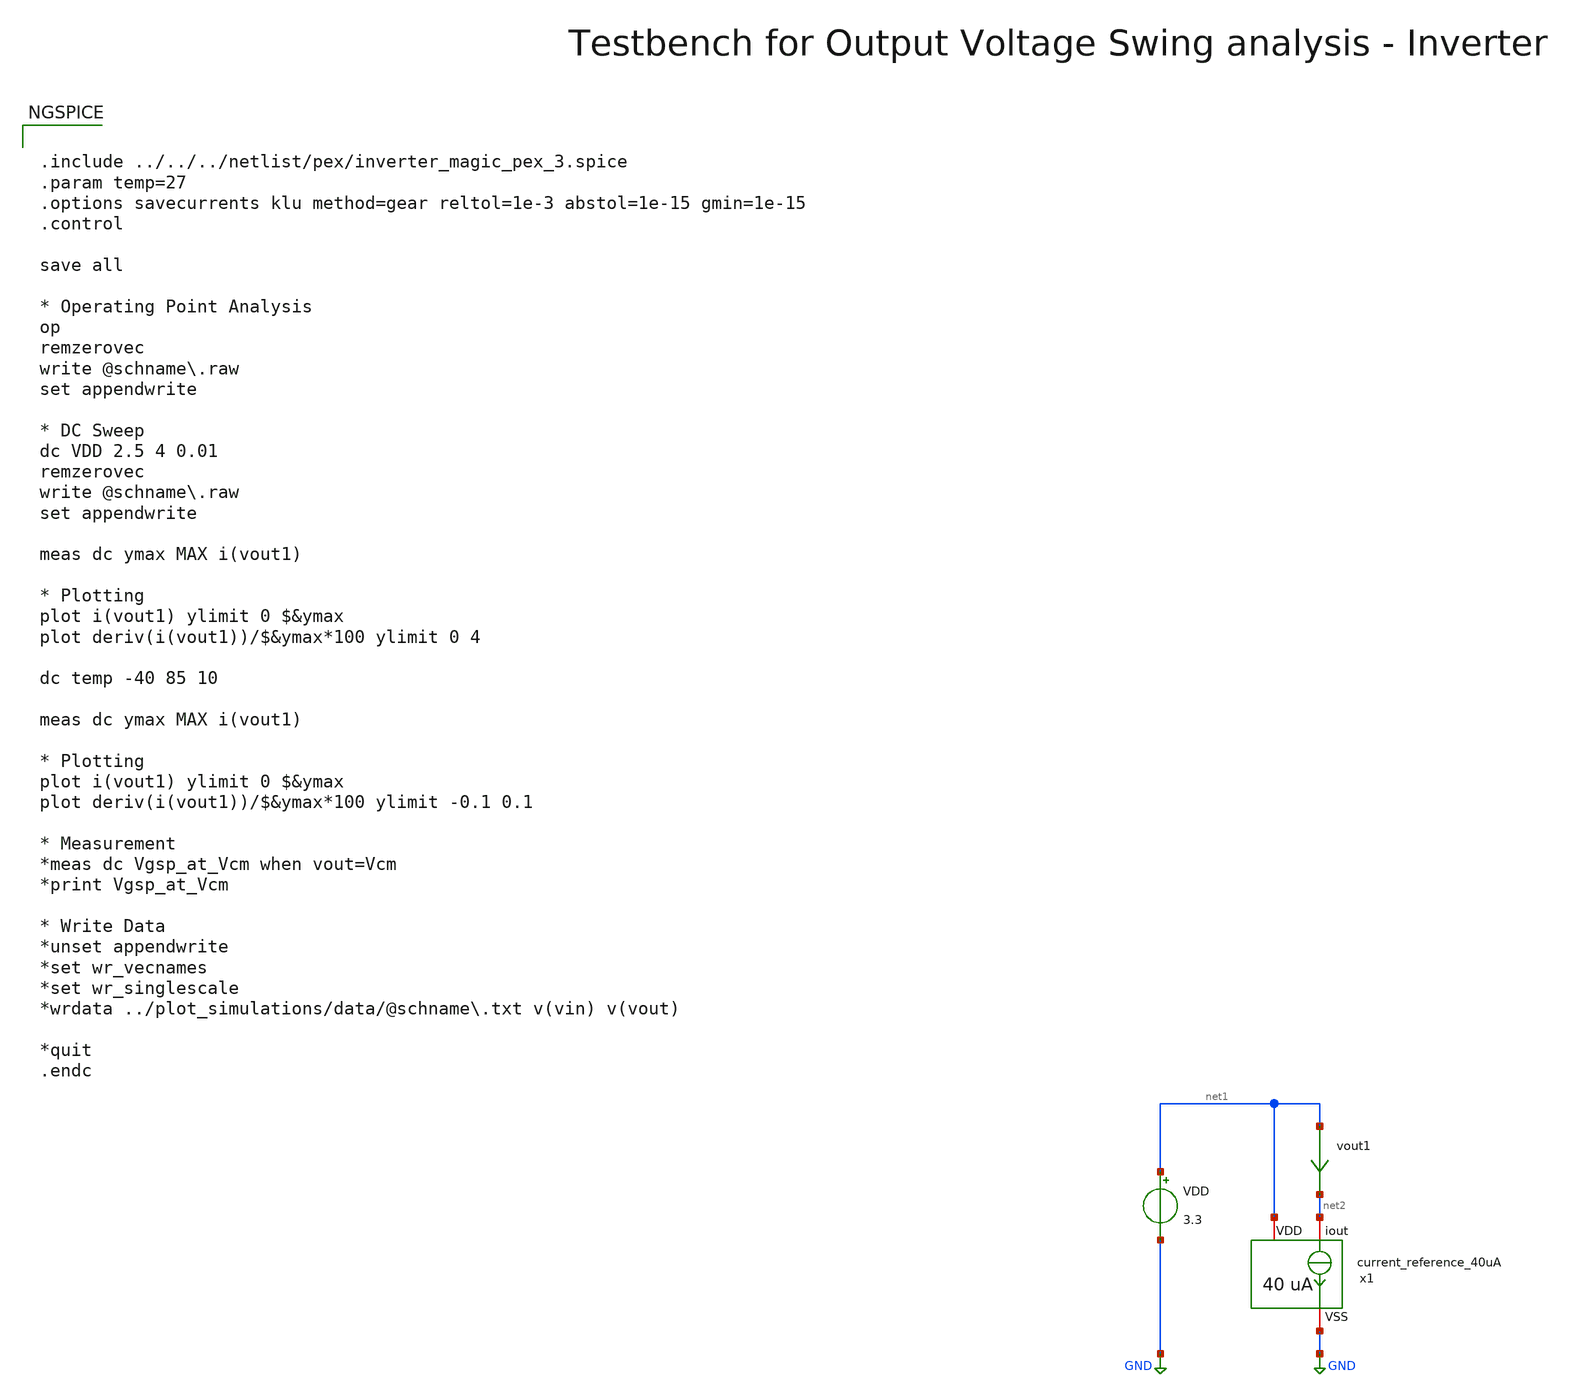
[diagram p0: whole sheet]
** sch_path: macros/heichips26_vcr/macros/switched_capacitor/testbenches/xschem/tb_current_reference_dc.sch
**.subckt tb_current_reference_dc
VDD net1 GND 3.3
vout1 net1 net2 0
.save i(vout1)
x1 net1 net2 GND current_reference_40uA
**** begin user architecture code


.include ../../../netlist/pex/inverter_magic_pex_3.spice
.param temp=27
.options savecurrents klu method=gear reltol=1e-3 abstol=1e-15 gmin=1e-15
.control

save all

* Operating Point Analysis
op
remzerovec
write @schname\.raw
set appendwrite

* DC Sweep
dc VDD 2.5 4 0.01
remzerovec
write @schname\.raw
set appendwrite

meas dc ymax MAX i(vout1)

* Plotting
plot i(vout1) ylimit 0 $&ymax
plot deriv(i(vout1))/$&ymax*100 ylimit 0 4

dc temp -40 85 10

meas dc ymax MAX i(vout1)

* Plotting
plot i(vout1) ylimit 0 $&ymax
plot deriv(i(vout1))/$&ymax*100 ylimit -0.1 0.1

* Measurement
*meas dc Vgsp_at_Vcm when vout=Vcm
*print Vgsp_at_Vcm

* Write Data
*unset appendwrite
*set wr_vecnames
*set wr_singlescale
*wrdata ../plot_simulations/data/@schname\.txt v(vin) v(vout)

*quit
.endc



.lib cornerMOSlv.lib mos_tt
.lib cornerMOShv.lib mos_tt
.lib cornerRES.lib res_typ
.lib cornerDIO.lib dio_tt

**** end user architecture code
**.ends

* expanding   symbol:  current_reference_40uA.sym # of pins=3
** sym_path: macros/heichips26_vcr/macros/switched_capacitor/schematic/xschem/current_reference_40uA.sym
** sch_path: macros/heichips26_vcr/macros/switched_capacitor/schematic/xschem/current_reference_40uA.sch
.subckt current_reference_40uA VDD iout VSS
*.iopin VSS
*.iopin VDD
*.iopin iout
XM8 net2 net2 VSS VSS sg13_hv_nmos w=n_w l=n_l ng=1 m=1 mm_ok=1
XM6 net2 net1 VDD VDD sg13_hv_pmos w=p_w l=p_l ng=1 m=1 mm_ok=1
XM1 net1 net1 VDD VDD sg13_hv_pmos w=p_w l=p_l ng=1 m=1 mm_ok=1
XM3 net1 net2 net3 VSS sg13_hv_nmos w=n_w l=n_l ng=1 m=1 mm_ok=1
XR2 net4 VSS VSS rppd w=2e-6 l=21.9e-6 m=1 b=0 mm_ok=1
XM2 net1 net2 net3 VSS sg13_hv_nmos w=n_w l=n_l ng=1 m=1 mm_ok=1
XM4 net1 net2 net3 VSS sg13_hv_nmos w=n_w l=n_l ng=1 m=1 mm_ok=1
XM5 net1 net2 net3 VSS sg13_hv_nmos w=n_w l=n_l ng=1 m=1 mm_ok=1
XM7 iout net2 VSS VSS sg13_hv_nmos w=n_w l=n_l ng=1 m=1 mm_ok=1
XR3 net3 net4 VSS rsil w=0.5e-6 l=365e-6 m=1 mm_ok=1
**** begin user architecture code


.param n_w = 6u
.param n_l = 5u
.param p_w = 10u
.param p_l = 2u


**** end user architecture code
.ends

.GLOBAL GND
.end
